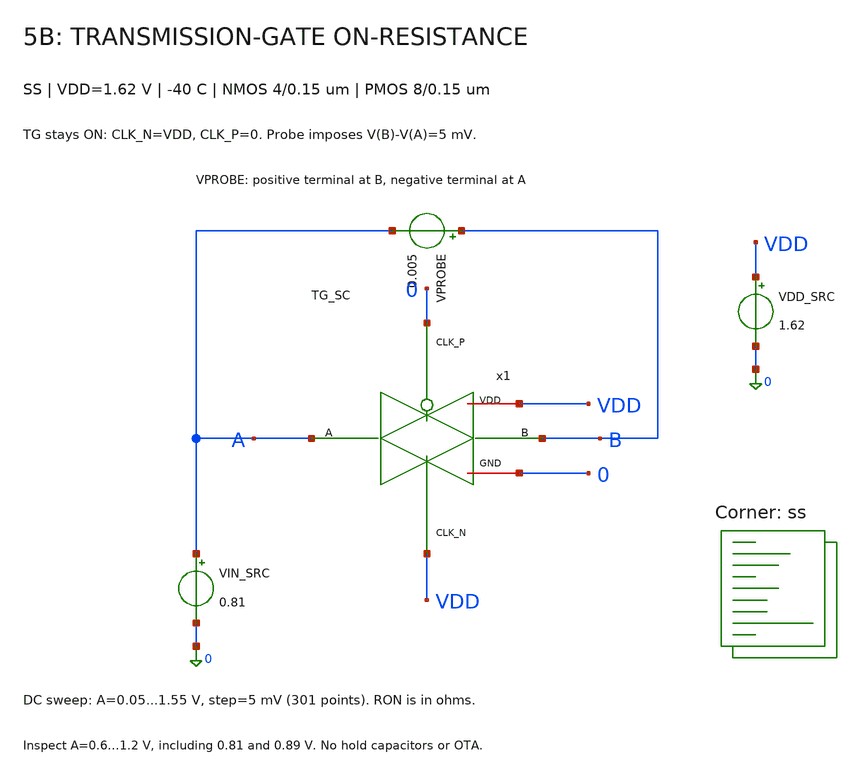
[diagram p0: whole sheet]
** sch_path: blocks/05_Switch_Network/sim/tb_5B_ron.sch
**.subckt tb_5B_ron
VPROBE B A 0.005
.save i(vprobe)
VIN_SRC A 0 0.81
VDD_SRC VDD 0 1.62
x1 A B 0 VDD VDD 0 TG_SC
**** begin user architecture code
.lib $::SKYWATER_MODELS/sky130.lib.spice ss


* DUT pin order: A B CLK_P CLK_N VDD GND.
* TG_SC.sch must contain WN=4 um, WP=8 um, L=0.15 um.
* Supply and NMOS gate: 1.62 V. PMOS gate: 0 V.
* Probe: VPROBE B A 0.005.
.option scale=1e-6 reltol=1e-5 abstol=1e-14 vntol=1e-8
.temp -40
.control
save all
set wr_singlescale
set wr_vecnames
set numdgt=15

dc VIN_SRC 0.05 1.55 0.005

let RON = abs((v(B)-v(A))/i(VPROBE))

meas dc RON_MIN MIN RON
meas dc RON_MAX MAX RON
meas dc RON_060 FIND RON AT=0.6
meas dc RON_081 FIND RON AT=0.81
meas dc RON_089 FIND RON AT=0.89
meas dc RON_090 FIND RON AT=0.9
meas dc RON_120 FIND RON AT=1.2

wrdata tb_5B_ron_ss_1p62_m40.dat v(A) v(B) i(VPROBE) RON
plot RON
.endc


**** end user architecture code
**.ends

* expanding   symbol:  blocks/05_Switch_Network/xschem/TG_SC.sym # of pins=6
** sym_path: blocks/05_Switch_Network/xschem/TG_SC.sym
** sch_path: blocks/05_Switch_Network/xschem/TG_SC.sch
.subckt TG_SC A B CLK_P CLK_N VDD GND
*.iopin A
*.iopin B
*.ipin CLK_P
*.ipin CLK_N
*.iopin VDD
*.iopin GND
XMP A CLK_P B VDD sky130_fd_pr__pfet_01v8 L=0.15 W=4 nf=1 ad='int((1 + 1)/2) * 4 / 1 * 0.29' as='int((1 + 2)/2) * 4 / 1 * 0.29'
+ pd='2*int((1 + 1)/2) * (4 / 1 + 0.29)' ps='2*int((1 + 2)/2) * (4 / 1 + 0.29)' nrd='0.29 / 4 ' nrs='0.29 / 4 '
+ sa=0 sb=0 sd=0 mult=1 m=1
XMN A CLK_N B GND sky130_fd_pr__nfet_01v8 L=0.15 W=2 nf=1 ad='int((1 + 1)/2) * 2 / 1 * 0.29' as='int((1 + 2)/2) * 2 / 1 * 0.29'
+ pd='2*int((1 + 1)/2) * (2 / 1 + 0.29)' ps='2*int((1 + 2)/2) * (2 / 1 + 0.29)' nrd='0.29 / 2 ' nrs='0.29 / 2 '
+ sa=0 sb=0 sd=0 mult=1 m=1
.ends

.end
